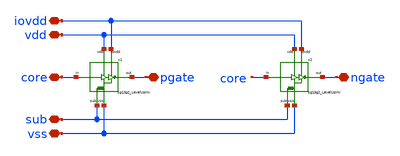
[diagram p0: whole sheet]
** sch_path: MSPHY6034-main/dependencies/unic_cass_2025_team04_padring/xschem/openpdk-libraries/ihp-sg13g2/sg13g2_io/xschem/sg13g2_GateLevelUpInv.sch
**.subckt sg13g2_GateLevelUpInv iovdd vss pgate core vdd sub ngate
*.iopin iovdd
*.iopin vss
*.iopin pgate
*.iopin core
*.iopin vdd
*.iopin sub
*.iopin ngate
x1 iovdd vss core pgate vdd sub sg13g2_LevelUpInv
x2 iovdd vss core ngate vdd sub sg13g2_LevelUpInv
**.ends

* expanding   symbol:  sg13g2_LevelUpInv.sym # of pins=6
** sym_path: MSPHY6034-main/dependencies/unic_cass_2025_team04_padring/xschem/openpdk-libraries/ihp-sg13g2/sg13g2_io/xschem/sg13g2_LevelUpInv.sym
** sch_path: MSPHY6034-main/dependencies/unic_cass_2025_team04_padring/xschem/openpdk-libraries/ihp-sg13g2/sg13g2_io/xschem/sg13g2_LevelUpInv.sch
.subckt sg13g2_LevelUpInv iovdd vss in out vdd sub
*.iopin iovdd
*.iopin vss
*.iopin out
*.iopin in
*.iopin vdd
*.iopin sub
XR1 vss sub ptap1 R=190.3 w=1.025e-6 l=1.025e-6
XM1 net1 in vss sub sg13_hv_nmos w=1.9u l=0.45u ng=1 m=1 mm_ok=1
XM3 net1 net2 iovdd iovdd sg13_hv_pmos w=0.3u l=0.45u ng=1 m=1 mm_ok=1
XM4 net2 net1 iovdd iovdd sg13_hv_pmos w=0.3u l=0.45u ng=1 m=1 mm_ok=1
XM5 out net2 iovdd iovdd sg13_hv_pmos w=3.9u l=0.45u ng=1 m=1 mm_ok=1
XM2 net2 net3 vss sub sg13_hv_nmos w=1.9u l=0.45u ng=1 m=1 mm_ok=1
XM6 out net2 vss sub sg13_hv_nmos w=1.9u l=0.45u ng=1 m=1 mm_ok=1
XM7 net3 in vss sub sg13_lv_nmos w=2.75u l=0.13u ng=1 m=1 mm_ok=1
XM8 net3 in vdd vdd sg13_lv_pmos w=4.75u l=0.13u ng=1 m=1 mm_ok=1
.ends

.end
